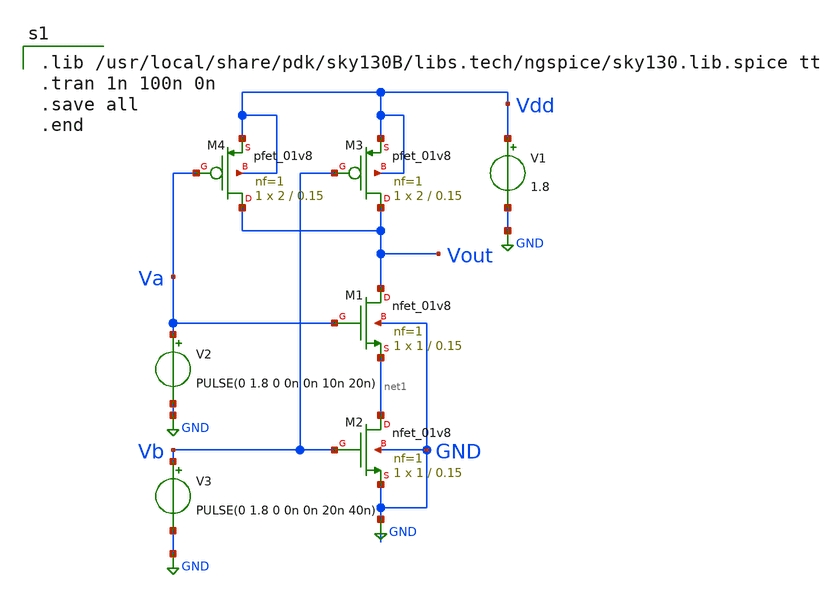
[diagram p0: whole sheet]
** sch_path: physical_design_layout_of_2_input_nand_gate/nand2gate_xschem.sch
**.subckt nand2gate_xschem
XM1 Vout Va net1 GND sky130_fd_pr__nfet_01v8 L=0.15 W=1 nf=1 ad='int((nf+1)/2) * W/nf * 0.29' as='int((nf+2)/2) * W/nf * 0.29'
+ pd='2*int((nf+1)/2) * (W/nf + 0.29)' ps='2*int((nf+2)/2) * (W/nf + 0.29)' nrd='0.29 / W' nrs='0.29 / W'
+ sa=0 sb=0 sd=0 mult=1 m=1
XM2 net1 Vb GND GND sky130_fd_pr__nfet_01v8 L=0.15 W=1 nf=1 ad='int((nf+1)/2) * W/nf * 0.29' as='int((nf+2)/2) * W/nf * 0.29'
+ pd='2*int((nf+1)/2) * (W/nf + 0.29)' ps='2*int((nf+2)/2) * (W/nf + 0.29)' nrd='0.29 / W' nrs='0.29 / W'
+ sa=0 sb=0 sd=0 mult=1 m=1
V1 Vdd GND 1.8
V2 Va GND PULSE(0 1.8 0 0n 0n 10n 20n)
V3 Vb GND PULSE(0 1.8 0 0n 0n 20n 40n)
XM3 Vout Vb Vdd Vdd sky130_fd_pr__pfet_01v8 L=0.15 W=2 nf=1 ad='int((nf+1)/2) * W/nf * 0.29' as='int((nf+2)/2) * W/nf * 0.29'
+ pd='2*int((nf+1)/2) * (W/nf + 0.29)' ps='2*int((nf+2)/2) * (W/nf + 0.29)' nrd='0.29 / W' nrs='0.29 / W'
+ sa=0 sb=0 sd=0 mult=1 m=1
XM4 Vout Va Vdd Vdd sky130_fd_pr__pfet_01v8 L=0.15 W=2 nf=1 ad='int((nf+1)/2) * W/nf * 0.29' as='int((nf+2)/2) * W/nf * 0.29'
+ pd='2*int((nf+1)/2) * (W/nf + 0.29)' ps='2*int((nf+2)/2) * (W/nf + 0.29)' nrd='0.29 / W' nrs='0.29 / W'
+ sa=0 sb=0 sd=0 mult=1 m=1
**** begin user architecture code

.lib /usr/local/share/pdk/sky130B/libs.tech/ngspice/sky130.lib.spice tt
.tran 1n 100n 0n
.save all
.end

**** end user architecture code
**.ends
.GLOBAL GND
.end
